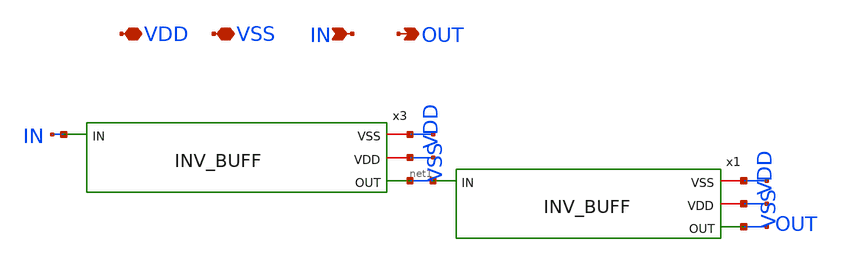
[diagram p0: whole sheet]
** sch_path: Clock_Generator_PAKISTAN_02/Schematics/Load_BUFF.sch
**.subckt Load_BUFF VDD VSS IN OUT
*.iopin VDD
*.iopin VSS
*.ipin IN
*.opin OUT
x3 VSS VDD net1 IN INV_BUFF
x1 VSS VDD OUT net1 INV_BUFF
**.ends
.end
